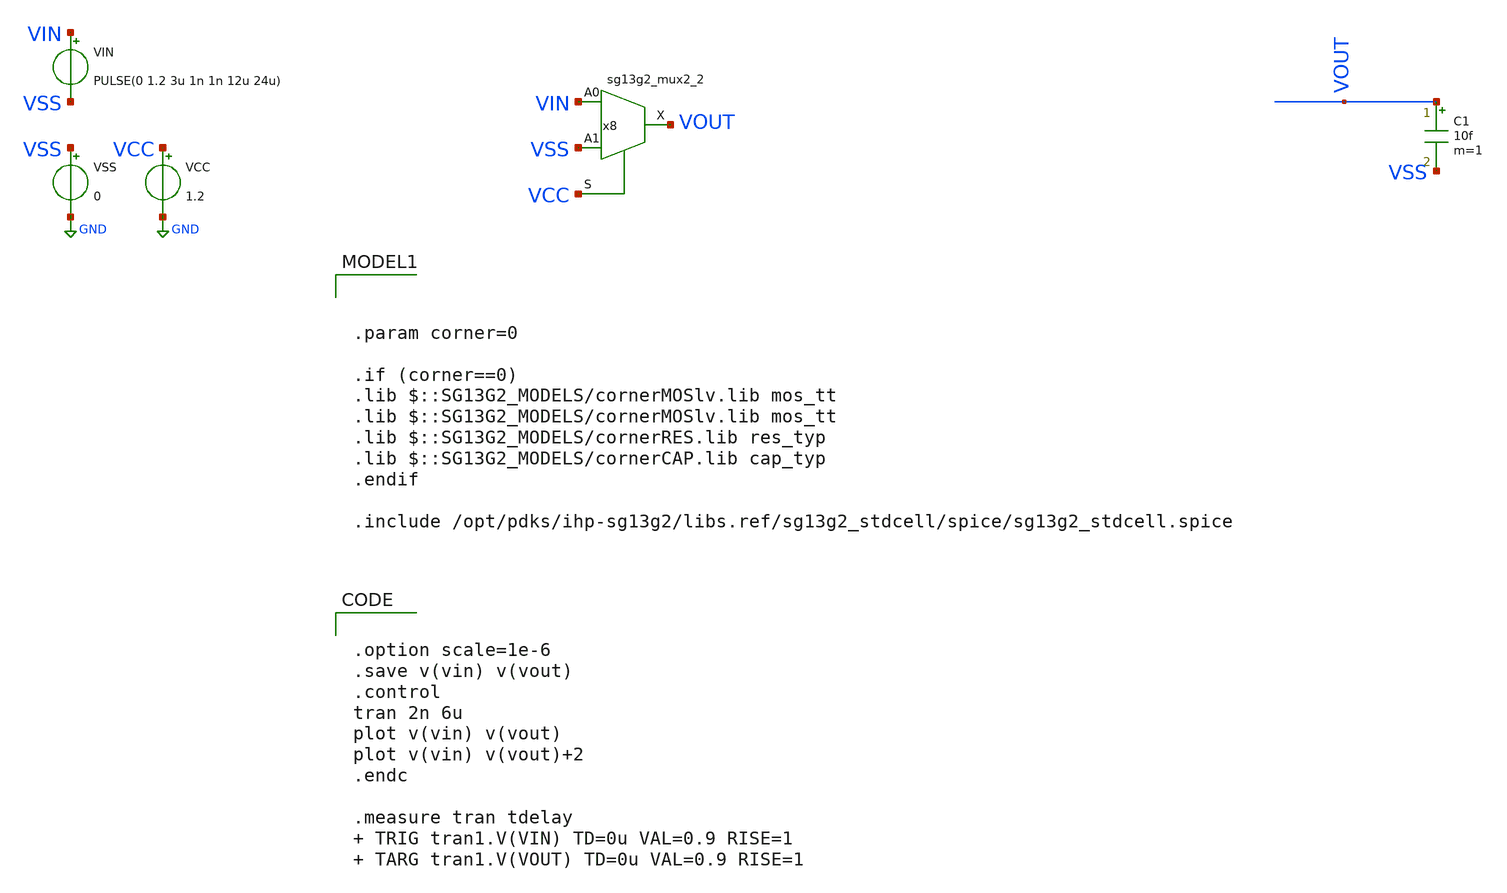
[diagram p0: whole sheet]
** sch_path: xschem/Digital_Block/tb_mux2_vto1p1.sch
**.subckt tb_mux2_vto1p1
VCC VCC GND 1.2
VSS VSS GND 0
VIN VIN VSS PULSE(0 1.2 3u 1n 1n 12u 24u)
C1 VOUT VSS 10f m=1
x8 VOUT VIN VSS VCC VCC VSS sg13g2_mux2_2
**** begin user architecture code


.option scale=1e-6
.save v(vin) v(vout)
.control
tran 2n 6u
plot v(vin) v(vout)
plot v(vin) v(vout)+2
.endc

.measure tran tdelay  TRIG tran1.V(VIN) TD=0u VAL=0.9 RISE=1  TARG tran1.V(VOUT) TD=0u VAL=0.9
+ RISE=1






.param corner=0

.if (corner==0)
.lib $::SG13G2_MODELS/cornerMOSlv.lib mos_tt
.lib $::SG13G2_MODELS/cornerMOSlv.lib mos_tt
.lib $::SG13G2_MODELS/cornerRES.lib res_typ
.lib $::SG13G2_MODELS/cornerCAP.lib cap_typ
.endif

.include /opt/pdks/ihp-sg13g2/libs.ref/sg13g2_stdcell/spice/sg13g2_stdcell.spice

**** end user architecture code
**.ends

* expanding   symbol:  sg13g2_stdcells/sg13g2_mux2_2.sym # of pins=4
** sym_path: sg13g2_stdcells/sg13g2_mux2_2.sym
** sch_path: sg13g2_stdcells/sg13g2_mux2_2.sch
.subckt sg13g2_mux2_2 X A0 A1 S VDD VSS
*.ipin S
*.ipin A0
*.ipin A1
*.opin X
*.iopin VDD
*.iopin VSS
XM1 Sb S VSS VSS sg13_lv_nmos w=550.00n l=130.00n ng=1 m=1 mm_ok=1
XM2 net1 A0 net5 VSS sg13_lv_nmos w=740.00n l=130.00n ng=1 m=1 mm_ok=1
XM3 net5 Sb VSS VSS sg13_lv_nmos w=740.00n l=130.00n ng=1 m=1 mm_ok=1
XM4 net1 A1 net4 VSS sg13_lv_nmos w=740.00n l=130.00n ng=1 m=1 mm_ok=1
XM5 net4 S VSS VSS sg13_lv_nmos w=740.00n l=130.00n ng=1 m=1 mm_ok=1
XM6 X net1 VSS VSS sg13_lv_nmos w=1.48u l=130.00n ng=2 m=1 mm_ok=1
XM7 Sb S VDD VDD sg13_lv_pmos w=840.00n l=130.00n ng=1 m=1 mm_ok=1
XM8 net2 S VDD VDD sg13_lv_pmos w=1.000u l=130.00n ng=1 m=1 mm_ok=1
XM9 net1 A0 net2 VDD sg13_lv_pmos w=1.000u l=130.00n ng=1 m=1 mm_ok=1
XM10 net3 Sb VDD VDD sg13_lv_pmos w=1.000u l=130.00n ng=1 m=1 mm_ok=1
XM11 net1 A1 net3 VDD sg13_lv_pmos w=1.000u l=130.00n ng=1 m=1 mm_ok=1
XM12 X net1 VDD VDD sg13_lv_pmos w=2.24u l=130.00n ng=2 m=1 mm_ok=1
.ends

.GLOBAL GND
.end
